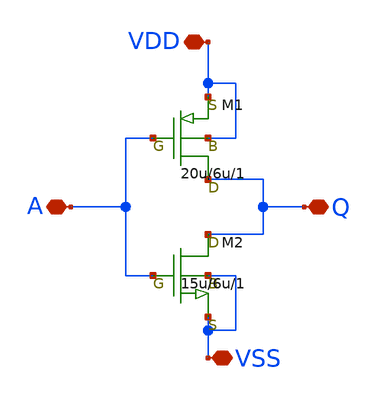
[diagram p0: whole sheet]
** sch_path: inverter.sch
**.subckt inverter A VDD Q VSS
*.iopin A
*.iopin VDD
*.iopin Q
*.iopin VSS
M1 Q A VDD VDD pch w=20u l=6u as=0 ps=0 ad=0 pd=0 m=1
M2 Q A VSS VSS nch w=15u l=6u as=0 ps=0 ad=0 pd=0 m=1
**.ends
.end
